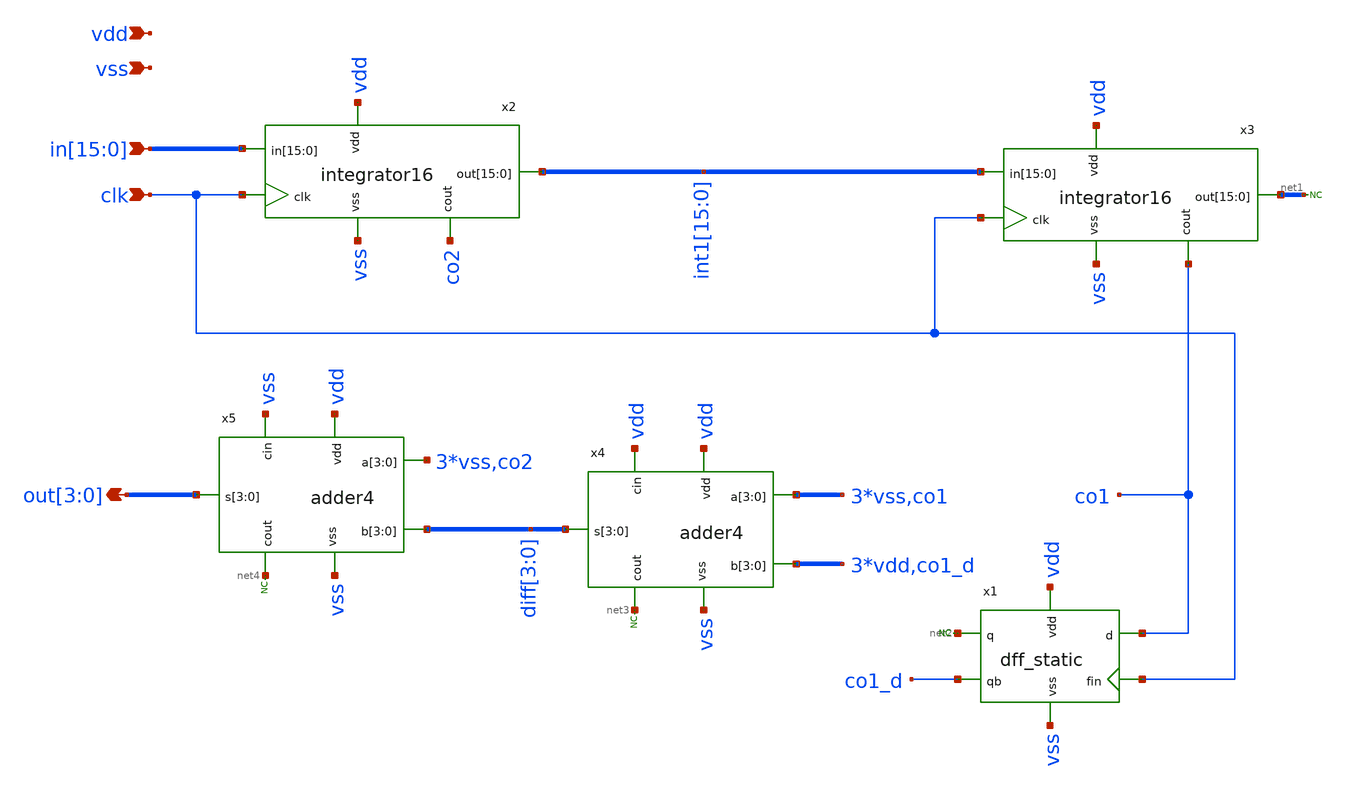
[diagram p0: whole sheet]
** sch_path: xschem/mash_1_1_dsm.sch
**.subckt mash_1_1_dsm
*+ in[15],in[14],in[13],in[12],in[11],in[10],in[9],in[8],in[7],in[6],in[5],in[4],in[3],in[2],in[1],in[0] vdd vss clk out[3],out[2],out[1],out[0]
*.ipin
*+ in[15],in[14],in[13],in[12],in[11],in[10],in[9],in[8],in[7],in[6],in[5],in[4],in[3],in[2],in[1],in[0]
*.ipin vdd
*.ipin vss
*.ipin clk
*.opin out[3],out[2],out[1],out[0]
x2 vdd vss in[15] in[14] in[13] in[12] in[11] in[10] in[9] in[8] in[7] in[6] in[5] in[4] in[3] in[2]
+ in[1] in[0] int1[15] int1[14] int1[13] int1[12] int1[11] int1[10] int1[9] int1[8] int1[7] int1[6] int1[5]
+ int1[4] int1[3] int1[2] int1[1] int1[0] clk co2 integrator16
x3 vdd vss int1[15] int1[14] int1[13] int1[12] int1[11] int1[10] int1[9] int1[8] int1[7] int1[6]
+ int1[5] int1[4] int1[3] int1[2] int1[1] int1[0] net1[15] net1[14] net1[13] net1[12] net1[11] net1[10]
+ net1[9] net1[8] net1[7] net1[6] net1[5] net1[4] net1[3] net1[2] net1[1] net1[0] clk co1 integrator16
* noconn #net1
x1 vdd co1_d net2 clk co1 vss dff_static
x4 vdd vdd vss vss vss vss co1 vdd vdd vdd co1_d diff[3] diff[2] diff[1] diff[0] net3 adder4
x5 vss vdd vss vss vss vss co2 diff[3] diff[2] diff[1] diff[0] out[3] out[2] out[1] out[0] net4
+ adder4
* noconn #net3
* noconn #net2
* noconn #net4
**.ends
.end
